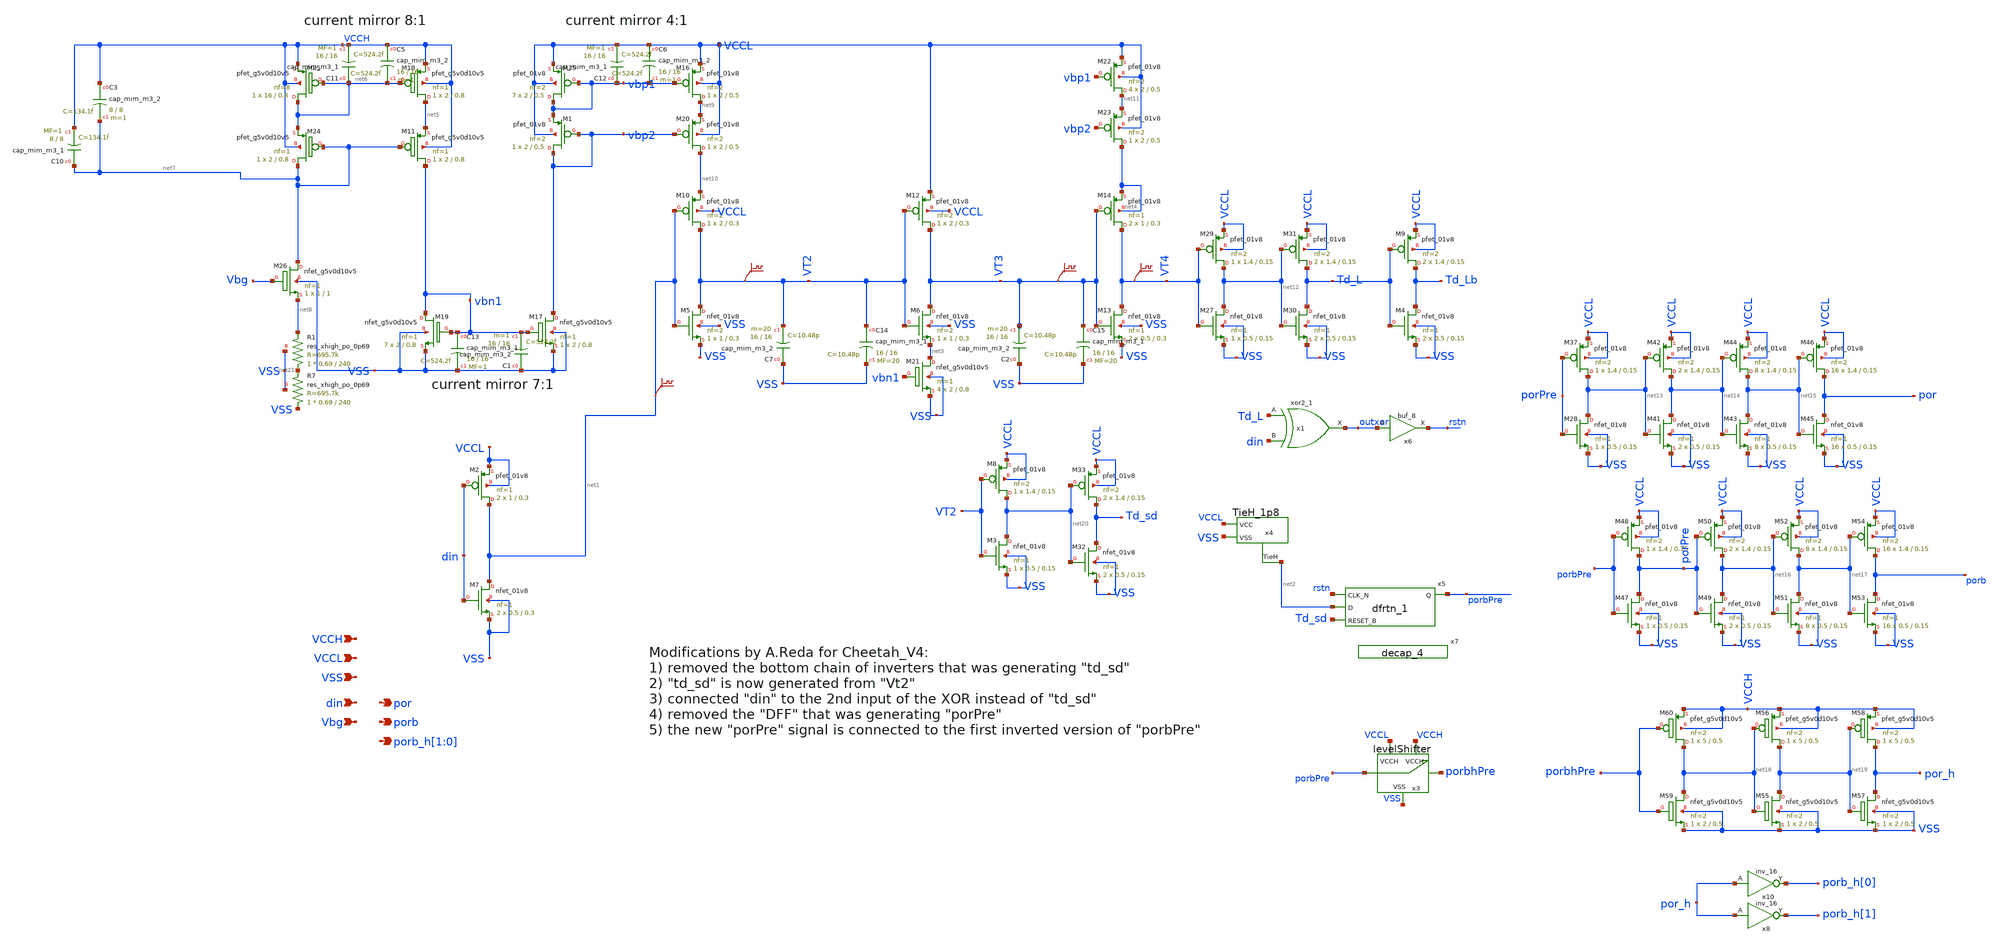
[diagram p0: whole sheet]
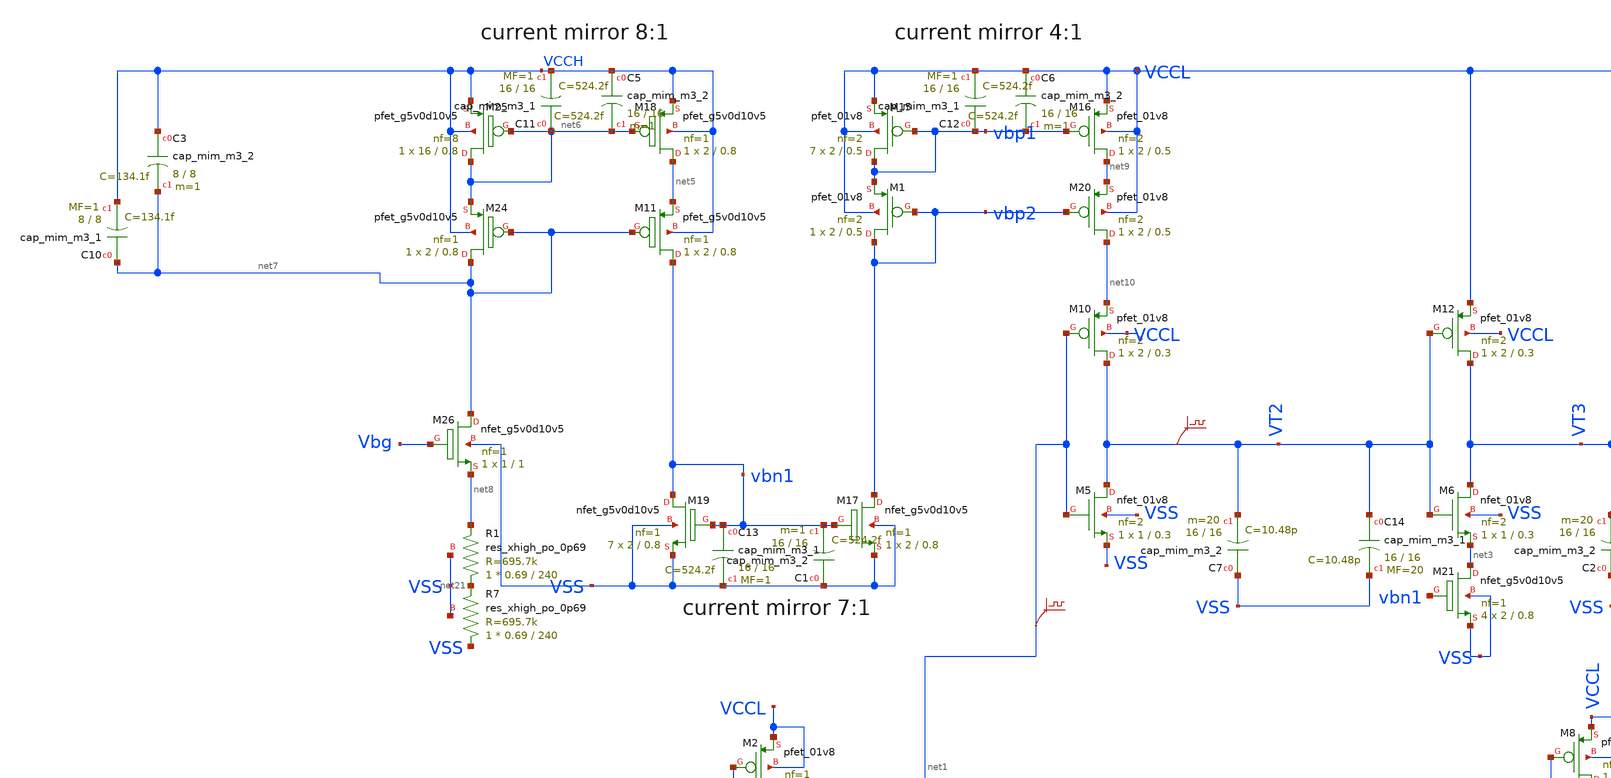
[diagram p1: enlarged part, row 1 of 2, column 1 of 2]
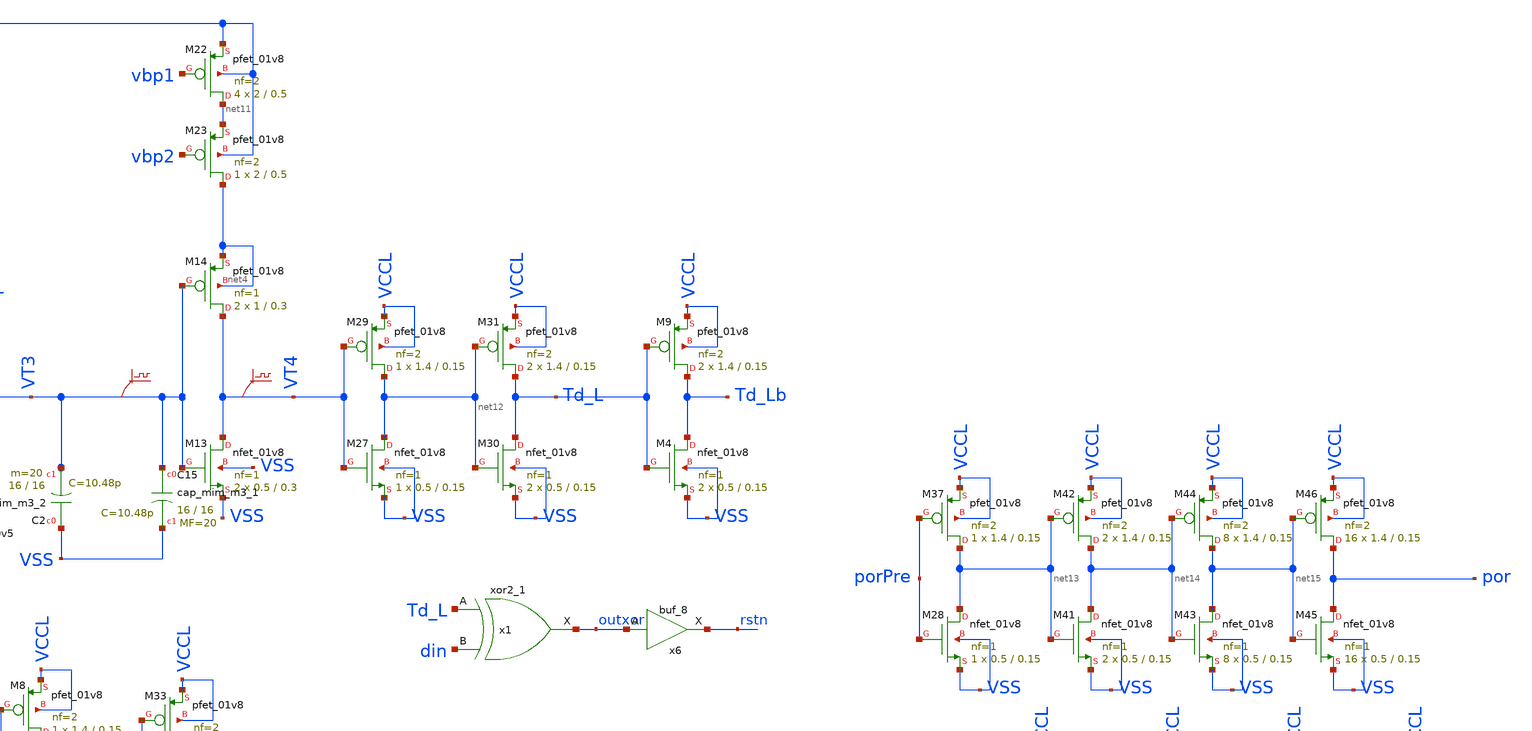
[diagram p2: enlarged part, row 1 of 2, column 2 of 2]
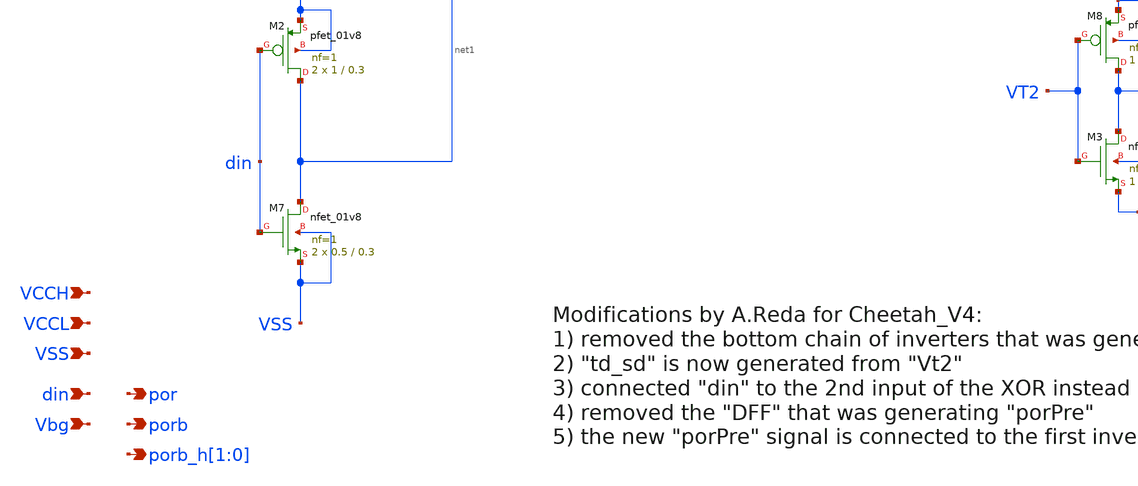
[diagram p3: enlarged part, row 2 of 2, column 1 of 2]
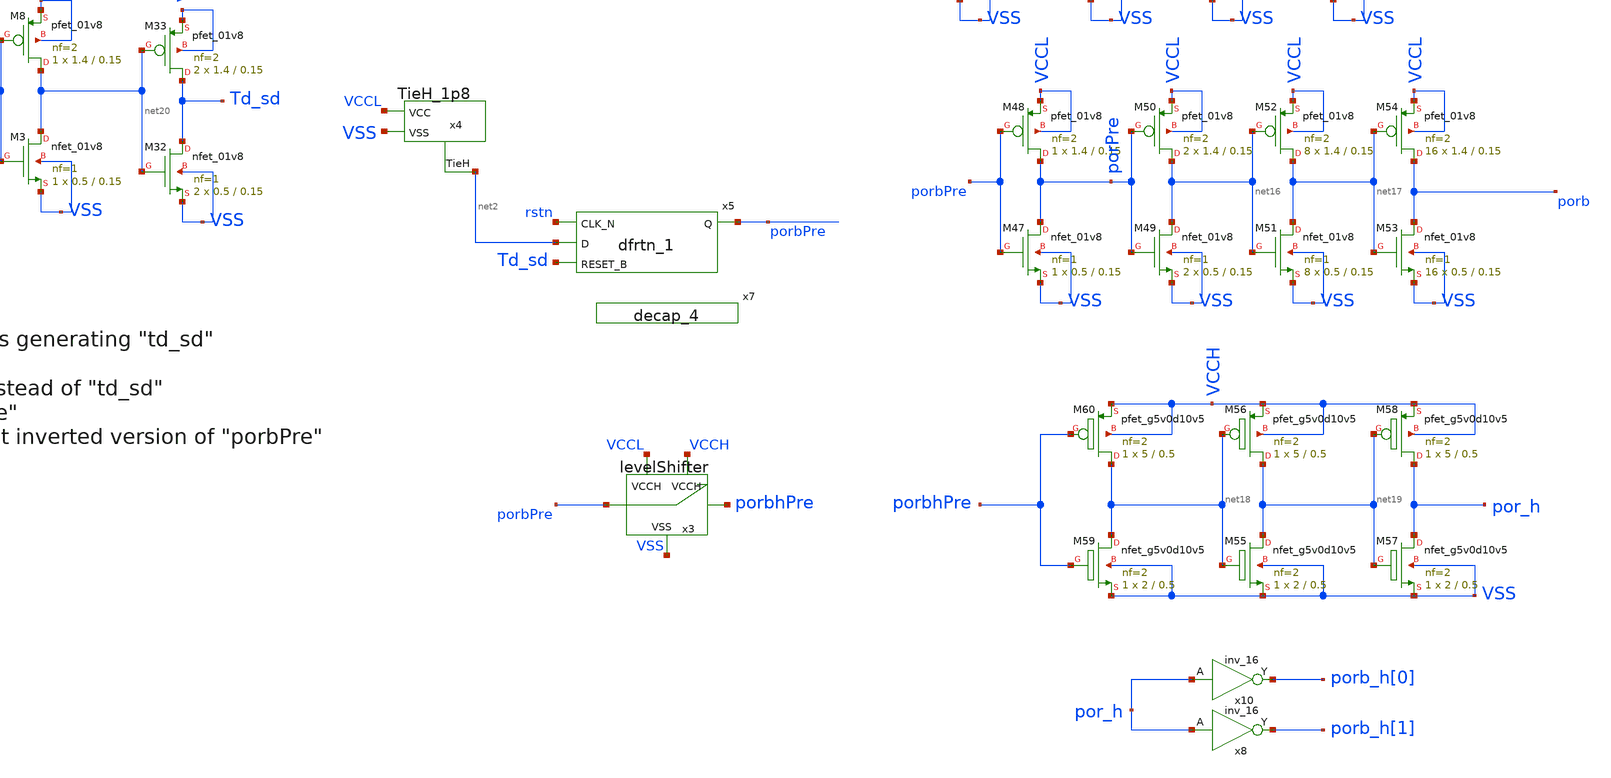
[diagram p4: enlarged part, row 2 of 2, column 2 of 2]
** sch_path: xschem/delayPulse_final.sch
**.subckt delayPulse_final VCCL VSS din Vbg por VCCH porb porb_h[1],porb_h[0]
*.ipin VCCL
*.ipin VSS
*.ipin din
*.ipin Vbg
*.opin por
*.ipin VCCH
*.opin porb
*.opin porb_h[1],porb_h[0]
x1 Td_L din VSS VSS VCCL VCCL outxor sky130_fd_sc_ls__xor2_1
x3 porbPre porbhPre VCCL VSS VCCH levelShifter
XM2 net1 din VCCL VCCL sky130_fd_pr__pfet_01v8 L=0.3 W=1 nf=1 ad='int((nf+1)/2) * W/nf * 0.29' as='int((nf+2)/2) * W/nf * 0.29'
+ pd='2*int((nf+1)/2) * (W/nf + 0.29)' ps='2*int((nf+2)/2) * (W/nf + 0.29)' nrd='0.29 / W' nrs='0.29 / W'
+ sa=0 sb=0 sd=0 mult=2 m=2
XM5 VT2 net1 VSS VSS sky130_fd_pr__nfet_01v8 L=0.3 W=1 nf=2 ad='int((nf+1)/2) * W/nf * 0.29' as='int((nf+2)/2) * W/nf * 0.29'
+ pd='2*int((nf+1)/2) * (W/nf + 0.29)' ps='2*int((nf+2)/2) * (W/nf + 0.29)' nrd='0.29 / W' nrs='0.29 / W'
+ sa=0 sb=0 sd=0 mult=1 m=1
XM7 net1 din VSS VSS sky130_fd_pr__nfet_01v8 L=0.3 W=0.5 nf=1 ad='int((nf+1)/2) * W/nf * 0.29' as='int((nf+2)/2) * W/nf * 0.29'
+ pd='2*int((nf+1)/2) * (W/nf + 0.29)' ps='2*int((nf+2)/2) * (W/nf + 0.29)' nrd='0.29 / W' nrs='0.29 / W'
+ sa=0 sb=0 sd=0 mult=2 m=2
XM10 VT2 net1 net10 VCCL sky130_fd_pr__pfet_01v8 L=0.3 W=2 nf=2 ad='int((nf+1)/2) * W/nf * 0.29' as='int((nf+2)/2) * W/nf * 0.29'
+ pd='2*int((nf+1)/2) * (W/nf + 0.29)' ps='2*int((nf+2)/2) * (W/nf + 0.29)' nrd='0.29 / W' nrs='0.29 / W'
+ sa=0 sb=0 sd=0 mult=1 m=1
XM13 VT4 VT3 VSS VSS sky130_fd_pr__nfet_01v8 L=0.3 W=0.5 nf=1 ad='int((nf+1)/2) * W/nf * 0.29' as='int((nf+2)/2) * W/nf * 0.29'
+ pd='2*int((nf+1)/2) * (W/nf + 0.29)' ps='2*int((nf+2)/2) * (W/nf + 0.29)' nrd='0.29 / W' nrs='0.29 / W'
+ sa=0 sb=0 sd=0 mult=2 m=2
XM14 VT4 VT3 net4 net4 sky130_fd_pr__pfet_01v8 L=0.3 W=1 nf=1 ad='int((nf+1)/2) * W/nf * 0.29' as='int((nf+2)/2) * W/nf * 0.29'
+ pd='2*int((nf+1)/2) * (W/nf + 0.29)' ps='2*int((nf+2)/2) * (W/nf + 0.29)' nrd='0.29 / W' nrs='0.29 / W'
+ sa=0 sb=0 sd=0 mult=2 m=2
x4 net2 VSS VCCL TieH_1p8
XM11 vbn1 net7 net5 VCCH sky130_fd_pr__pfet_g5v0d10v5 L=0.8 W=2 nf=1 ad='int((nf+1)/2) * W/nf * 0.29'
+ as='int((nf+2)/2) * W/nf * 0.29' pd='2*int((nf+1)/2) * (W/nf + 0.29)' ps='2*int((nf+2)/2) * (W/nf + 0.29)'
+ nrd='0.29 / W' nrs='0.29 / W' sa=0 sb=0 sd=0 mult=1 m=1
XM17 vbp2 vbn1 VSS VSS sky130_fd_pr__nfet_g5v0d10v5 L=0.8 W=2 nf=1 ad='int((nf+1)/2) * W/nf * 0.29' as='int((nf+2)/2) * W/nf * 0.29'
+ pd='2*int((nf+1)/2) * (W/nf + 0.29)' ps='2*int((nf+2)/2) * (W/nf + 0.29)' nrd='0.29 / W' nrs='0.29 / W'
+ sa=0 sb=0 sd=0 mult=1 m=1
XM18 net5 net6 VCCH VCCH sky130_fd_pr__pfet_g5v0d10v5 L=0.8 W=2 nf=1 ad='int((nf+1)/2) * W/nf * 0.29'
+ as='int((nf+2)/2) * W/nf * 0.29' pd='2*int((nf+1)/2) * (W/nf + 0.29)' ps='2*int((nf+2)/2) * (W/nf + 0.29)'
+ nrd='0.29 / W' nrs='0.29 / W' sa=0 sb=0 sd=0 mult=1 m=1
XM19 vbn1 vbn1 VSS VSS sky130_fd_pr__nfet_g5v0d10v5 L=0.8 W=2 nf=1 ad='int((nf+1)/2) * W/nf * 0.29' as='int((nf+2)/2) * W/nf * 0.29'
+ pd='2*int((nf+1)/2) * (W/nf + 0.29)' ps='2*int((nf+2)/2) * (W/nf + 0.29)' nrd='0.29 / W' nrs='0.29 / W'
+ sa=0 sb=0 sd=0 mult=7 m=7
XM24 net7 net7 net6 VCCH sky130_fd_pr__pfet_g5v0d10v5 L=0.8 W=2 nf=1 ad='int((nf+1)/2) * W/nf * 0.29'
+ as='int((nf+2)/2) * W/nf * 0.29' pd='2*int((nf+1)/2) * (W/nf + 0.29)' ps='2*int((nf+2)/2) * (W/nf + 0.29)'
+ nrd='0.29 / W' nrs='0.29 / W' sa=0 sb=0 sd=0 mult=1 m=1
XM25 net6 net6 VCCH VCCH sky130_fd_pr__pfet_g5v0d10v5 L=0.8 W=16 nf=8 ad='int((nf+1)/2) * W/nf * 0.29'
+ as='int((nf+2)/2) * W/nf * 0.29' pd='2*int((nf+1)/2) * (W/nf + 0.29)' ps='2*int((nf+2)/2) * (W/nf + 0.29)'
+ nrd='0.29 / W' nrs='0.29 / W' sa=0 sb=0 sd=0 mult=1 m=1
XM26 net7 Vbg net8 VSS sky130_fd_pr__nfet_g5v0d10v5 L=1 W=1 nf=1 ad='int((nf+1)/2) * W/nf * 0.29' as='int((nf+2)/2) * W/nf * 0.29'
+ pd='2*int((nf+1)/2) * (W/nf + 0.29)' ps='2*int((nf+2)/2) * (W/nf + 0.29)' nrd='0.29 / W' nrs='0.29 / W'
+ sa=0 sb=0 sd=0 mult=1 m=1
XM6 VT3 VT2 net3 VSS sky130_fd_pr__nfet_01v8 L=0.3 W=1 nf=2 ad='int((nf+1)/2) * W/nf * 0.29' as='int((nf+2)/2) * W/nf * 0.29'
+ pd='2*int((nf+1)/2) * (W/nf + 0.29)' ps='2*int((nf+2)/2) * (W/nf + 0.29)' nrd='0.29 / W' nrs='0.29 / W'
+ sa=0 sb=0 sd=0 mult=1 m=1
XM12 VT3 VT2 VCCL VCCL sky130_fd_pr__pfet_01v8 L=0.3 W=2 nf=2 ad='int((nf+1)/2) * W/nf * 0.29' as='int((nf+2)/2) * W/nf * 0.29'
+ pd='2*int((nf+1)/2) * (W/nf + 0.29)' ps='2*int((nf+2)/2) * (W/nf + 0.29)' nrd='0.29 / W' nrs='0.29 / W'
+ sa=0 sb=0 sd=0 mult=1 m=1
XM1 vbp2 vbp2 vbp1 VCCL sky130_fd_pr__pfet_01v8 L=0.5 W=2 nf=2 ad='int((nf+1)/2) * W/nf * 0.29' as='int((nf+2)/2) * W/nf * 0.29'
+ pd='2*int((nf+1)/2) * (W/nf + 0.29)' ps='2*int((nf+2)/2) * (W/nf + 0.29)' nrd='0.29 / W' nrs='0.29 / W'
+ sa=0 sb=0 sd=0 mult=1 m=1
XM15 vbp1 vbp1 VCCL VCCL sky130_fd_pr__pfet_01v8 L=0.5 W=2 nf=2 ad='int((nf+1)/2) * W/nf * 0.29' as='int((nf+2)/2) * W/nf * 0.29'
+ pd='2*int((nf+1)/2) * (W/nf + 0.29)' ps='2*int((nf+2)/2) * (W/nf + 0.29)' nrd='0.29 / W' nrs='0.29 / W'
+ sa=0 sb=0 sd=0 mult=7 m=7
XM16 net9 vbp1 VCCL VCCL sky130_fd_pr__pfet_01v8 L=0.5 W=2 nf=2 ad='int((nf+1)/2) * W/nf * 0.29' as='int((nf+2)/2) * W/nf * 0.29'
+ pd='2*int((nf+1)/2) * (W/nf + 0.29)' ps='2*int((nf+2)/2) * (W/nf + 0.29)' nrd='0.29 / W' nrs='0.29 / W'
+ sa=0 sb=0 sd=0 mult=1 m=1
XM20 net10 vbp2 net9 VCCL sky130_fd_pr__pfet_01v8 L=0.5 W=2 nf=2 ad='int((nf+1)/2) * W/nf * 0.29' as='int((nf+2)/2) * W/nf * 0.29'
+ pd='2*int((nf+1)/2) * (W/nf + 0.29)' ps='2*int((nf+2)/2) * (W/nf + 0.29)' nrd='0.29 / W' nrs='0.29 / W'
+ sa=0 sb=0 sd=0 mult=1 m=1
XM21 net3 vbn1 VSS VSS sky130_fd_pr__nfet_g5v0d10v5 L=0.8 W=2 nf=1 ad='int((nf+1)/2) * W/nf * 0.29' as='int((nf+2)/2) * W/nf * 0.29'
+ pd='2*int((nf+1)/2) * (W/nf + 0.29)' ps='2*int((nf+2)/2) * (W/nf + 0.29)' nrd='0.29 / W' nrs='0.29 / W'
+ sa=0 sb=0 sd=0 mult=4 m=4
XM22 net11 vbp1 VCCL VCCL sky130_fd_pr__pfet_01v8 L=0.5 W=2 nf=2 ad='int((nf+1)/2) * W/nf * 0.29' as='int((nf+2)/2) * W/nf * 0.29'
+ pd='2*int((nf+1)/2) * (W/nf + 0.29)' ps='2*int((nf+2)/2) * (W/nf + 0.29)' nrd='0.29 / W' nrs='0.29 / W'
+ sa=0 sb=0 sd=0 mult=4 m=4
XM23 net4 vbp2 net11 VCCL sky130_fd_pr__pfet_01v8 L=0.5 W=2 nf=2 ad='int((nf+1)/2) * W/nf * 0.29' as='int((nf+2)/2) * W/nf * 0.29'
+ pd='2*int((nf+1)/2) * (W/nf + 0.29)' ps='2*int((nf+2)/2) * (W/nf + 0.29)' nrd='0.29 / W' nrs='0.29 / W'
+ sa=0 sb=0 sd=0 mult=1 m=1
XM27 net12 VT4 VSS VSS sky130_fd_pr__nfet_01v8 L=0.15 W=0.5 nf=1 ad='int((nf+1)/2) * W/nf * 0.29' as='int((nf+2)/2) * W/nf * 0.29'
+ pd='2*int((nf+1)/2) * (W/nf + 0.29)' ps='2*int((nf+2)/2) * (W/nf + 0.29)' nrd='0.29 / W' nrs='0.29 / W'
+ sa=0 sb=0 sd=0 mult=1 m=1
XM29 net12 VT4 VCCL VCCL sky130_fd_pr__pfet_01v8 L=0.15 W=1.4 nf=2 ad='int((nf+1)/2) * W/nf * 0.29' as='int((nf+2)/2) * W/nf * 0.29'
+ pd='2*int((nf+1)/2) * (W/nf + 0.29)' ps='2*int((nf+2)/2) * (W/nf + 0.29)' nrd='0.29 / W' nrs='0.29 / W'
+ sa=0 sb=0 sd=0 mult=1 m=1
XM30 Td_L net12 VSS VSS sky130_fd_pr__nfet_01v8 L=0.15 W=0.5 nf=1 ad='int((nf+1)/2) * W/nf * 0.29' as='int((nf+2)/2) * W/nf * 0.29'
+ pd='2*int((nf+1)/2) * (W/nf + 0.29)' ps='2*int((nf+2)/2) * (W/nf + 0.29)' nrd='0.29 / W' nrs='0.29 / W'
+ sa=0 sb=0 sd=0 mult=2 m=2
XM31 Td_L net12 VCCL VCCL sky130_fd_pr__pfet_01v8 L=0.15 W=1.4 nf=2 ad='int((nf+1)/2) * W/nf * 0.29'
+ as='int((nf+2)/2) * W/nf * 0.29' pd='2*int((nf+1)/2) * (W/nf + 0.29)' ps='2*int((nf+2)/2) * (W/nf + 0.29)'
+ nrd='0.29 / W' nrs='0.29 / W' sa=0 sb=0 sd=0 mult=2 m=2
x6 outxor VSS VSS VCCL VCCL rstn sky130_fd_sc_ls__buf_8
XC7 VSS VT2 sky130_fd_pr__cap_mim_m3_2 W=16 L=16 MF=20 m=20
XC2 VSS VT3 sky130_fd_pr__cap_mim_m3_2 W=16 L=16 MF=20 m=20
x5 rstn net2 Td_sd VSS VSS VCCL VCCL porbPre sky130_fd_sc_ls__dfrtn_1
XM4 Td_Lb Td_L VSS VSS sky130_fd_pr__nfet_01v8 L=0.15 W=0.5 nf=1 ad='int((nf+1)/2) * W/nf * 0.29' as='int((nf+2)/2) * W/nf * 0.29'
+ pd='2*int((nf+1)/2) * (W/nf + 0.29)' ps='2*int((nf+2)/2) * (W/nf + 0.29)' nrd='0.29 / W' nrs='0.29 / W'
+ sa=0 sb=0 sd=0 mult=2 m=2
XM9 Td_Lb Td_L VCCL VCCL sky130_fd_pr__pfet_01v8 L=0.15 W=1.4 nf=2 ad='int((nf+1)/2) * W/nf * 0.29' as='int((nf+2)/2) * W/nf * 0.29'
+ pd='2*int((nf+1)/2) * (W/nf + 0.29)' ps='2*int((nf+2)/2) * (W/nf + 0.29)' nrd='0.29 / W' nrs='0.29 / W'
+ sa=0 sb=0 sd=0 mult=2 m=2
XC1 VSS vbn1 sky130_fd_pr__cap_mim_m3_2 W=16 L=16 MF=1 m=1
XC5 VCCH net6 sky130_fd_pr__cap_mim_m3_2 W=16 L=16 MF=1 m=1
XC6 VCCL vbp1 sky130_fd_pr__cap_mim_m3_2 W=16 L=16 MF=1 m=1
XC3 VCCH net7 sky130_fd_pr__cap_mim_m3_2 W=8 L=8 MF=1 m=1
XM28 net13 porPre VSS VSS sky130_fd_pr__nfet_01v8 L=0.15 W=0.5 nf=1 ad='int((nf+1)/2) * W/nf * 0.29'
+ as='int((nf+2)/2) * W/nf * 0.29' pd='2*int((nf+1)/2) * (W/nf + 0.29)' ps='2*int((nf+2)/2) * (W/nf + 0.29)'
+ nrd='0.29 / W' nrs='0.29 / W' sa=0 sb=0 sd=0 mult=1 m=1
XM37 net13 porPre VCCL VCCL sky130_fd_pr__pfet_01v8 L=0.15 W=1.4 nf=2 ad='int((nf+1)/2) * W/nf * 0.29'
+ as='int((nf+2)/2) * W/nf * 0.29' pd='2*int((nf+1)/2) * (W/nf + 0.29)' ps='2*int((nf+2)/2) * (W/nf + 0.29)'
+ nrd='0.29 / W' nrs='0.29 / W' sa=0 sb=0 sd=0 mult=1 m=1
XM41 net14 net13 VSS VSS sky130_fd_pr__nfet_01v8 L=0.15 W=0.5 nf=1 ad='int((nf+1)/2) * W/nf * 0.29' as='int((nf+2)/2) * W/nf * 0.29'
+ pd='2*int((nf+1)/2) * (W/nf + 0.29)' ps='2*int((nf+2)/2) * (W/nf + 0.29)' nrd='0.29 / W' nrs='0.29 / W'
+ sa=0 sb=0 sd=0 mult=2 m=2
XM42 net14 net13 VCCL VCCL sky130_fd_pr__pfet_01v8 L=0.15 W=1.4 nf=2 ad='int((nf+1)/2) * W/nf * 0.29'
+ as='int((nf+2)/2) * W/nf * 0.29' pd='2*int((nf+1)/2) * (W/nf + 0.29)' ps='2*int((nf+2)/2) * (W/nf + 0.29)'
+ nrd='0.29 / W' nrs='0.29 / W' sa=0 sb=0 sd=0 mult=2 m=2
XM43 net15 net14 VSS VSS sky130_fd_pr__nfet_01v8 L=0.15 W=0.5 nf=1 ad='int((nf+1)/2) * W/nf * 0.29' as='int((nf+2)/2) * W/nf * 0.29'
+ pd='2*int((nf+1)/2) * (W/nf + 0.29)' ps='2*int((nf+2)/2) * (W/nf + 0.29)' nrd='0.29 / W' nrs='0.29 / W'
+ sa=0 sb=0 sd=0 mult=8 m=8
XM44 net15 net14 VCCL VCCL sky130_fd_pr__pfet_01v8 L=0.15 W=1.4 nf=2 ad='int((nf+1)/2) * W/nf * 0.29'
+ as='int((nf+2)/2) * W/nf * 0.29' pd='2*int((nf+1)/2) * (W/nf + 0.29)' ps='2*int((nf+2)/2) * (W/nf + 0.29)'
+ nrd='0.29 / W' nrs='0.29 / W' sa=0 sb=0 sd=0 mult=8 m=8
XM45 por net15 VSS VSS sky130_fd_pr__nfet_01v8 L=0.15 W=0.5 nf=1 ad='int((nf+1)/2) * W/nf * 0.29' as='int((nf+2)/2) * W/nf * 0.29'
+ pd='2*int((nf+1)/2) * (W/nf + 0.29)' ps='2*int((nf+2)/2) * (W/nf + 0.29)' nrd='0.29 / W' nrs='0.29 / W'
+ sa=0 sb=0 sd=0 mult=16 m=16
XM46 por net15 VCCL VCCL sky130_fd_pr__pfet_01v8 L=0.15 W=1.4 nf=2 ad='int((nf+1)/2) * W/nf * 0.29' as='int((nf+2)/2) * W/nf * 0.29'
+ pd='2*int((nf+1)/2) * (W/nf + 0.29)' ps='2*int((nf+2)/2) * (W/nf + 0.29)' nrd='0.29 / W' nrs='0.29 / W'
+ sa=0 sb=0 sd=0 mult=16 m=16
XM47 porPre porbPre VSS VSS sky130_fd_pr__nfet_01v8 L=0.15 W=0.5 nf=1 ad='int((nf+1)/2) * W/nf * 0.29'
+ as='int((nf+2)/2) * W/nf * 0.29' pd='2*int((nf+1)/2) * (W/nf + 0.29)' ps='2*int((nf+2)/2) * (W/nf + 0.29)'
+ nrd='0.29 / W' nrs='0.29 / W' sa=0 sb=0 sd=0 mult=1 m=1
XM48 porPre porbPre VCCL VCCL sky130_fd_pr__pfet_01v8 L=0.15 W=1.4 nf=2 ad='int((nf+1)/2) * W/nf * 0.29'
+ as='int((nf+2)/2) * W/nf * 0.29' pd='2*int((nf+1)/2) * (W/nf + 0.29)' ps='2*int((nf+2)/2) * (W/nf + 0.29)'
+ nrd='0.29 / W' nrs='0.29 / W' sa=0 sb=0 sd=0 mult=1 m=1
XM49 net16 porPre VSS VSS sky130_fd_pr__nfet_01v8 L=0.15 W=0.5 nf=1 ad='int((nf+1)/2) * W/nf * 0.29'
+ as='int((nf+2)/2) * W/nf * 0.29' pd='2*int((nf+1)/2) * (W/nf + 0.29)' ps='2*int((nf+2)/2) * (W/nf + 0.29)'
+ nrd='0.29 / W' nrs='0.29 / W' sa=0 sb=0 sd=0 mult=2 m=2
XM50 net16 porPre VCCL VCCL sky130_fd_pr__pfet_01v8 L=0.15 W=1.4 nf=2 ad='int((nf+1)/2) * W/nf * 0.29'
+ as='int((nf+2)/2) * W/nf * 0.29' pd='2*int((nf+1)/2) * (W/nf + 0.29)' ps='2*int((nf+2)/2) * (W/nf + 0.29)'
+ nrd='0.29 / W' nrs='0.29 / W' sa=0 sb=0 sd=0 mult=2 m=2
XM51 net17 net16 VSS VSS sky130_fd_pr__nfet_01v8 L=0.15 W=0.5 nf=1 ad='int((nf+1)/2) * W/nf * 0.29' as='int((nf+2)/2) * W/nf * 0.29'
+ pd='2*int((nf+1)/2) * (W/nf + 0.29)' ps='2*int((nf+2)/2) * (W/nf + 0.29)' nrd='0.29 / W' nrs='0.29 / W'
+ sa=0 sb=0 sd=0 mult=8 m=8
XM52 net17 net16 VCCL VCCL sky130_fd_pr__pfet_01v8 L=0.15 W=1.4 nf=2 ad='int((nf+1)/2) * W/nf * 0.29'
+ as='int((nf+2)/2) * W/nf * 0.29' pd='2*int((nf+1)/2) * (W/nf + 0.29)' ps='2*int((nf+2)/2) * (W/nf + 0.29)'
+ nrd='0.29 / W' nrs='0.29 / W' sa=0 sb=0 sd=0 mult=8 m=8
XM53 porb net17 VSS VSS sky130_fd_pr__nfet_01v8 L=0.15 W=0.5 nf=1 ad='int((nf+1)/2) * W/nf * 0.29' as='int((nf+2)/2) * W/nf * 0.29'
+ pd='2*int((nf+1)/2) * (W/nf + 0.29)' ps='2*int((nf+2)/2) * (W/nf + 0.29)' nrd='0.29 / W' nrs='0.29 / W'
+ sa=0 sb=0 sd=0 mult=16 m=16
XM54 porb net17 VCCL VCCL sky130_fd_pr__pfet_01v8 L=0.15 W=1.4 nf=2 ad='int((nf+1)/2) * W/nf * 0.29'
+ as='int((nf+2)/2) * W/nf * 0.29' pd='2*int((nf+1)/2) * (W/nf + 0.29)' ps='2*int((nf+2)/2) * (W/nf + 0.29)'
+ nrd='0.29 / W' nrs='0.29 / W' sa=0 sb=0 sd=0 mult=16 m=16
XM59 net18 porbhPre VSS VSS sky130_fd_pr__nfet_g5v0d10v5 L=0.5 W=2 nf=2 ad='int((nf+1)/2) * W/nf * 0.29'
+ as='int((nf+2)/2) * W/nf * 0.29' pd='2*int((nf+1)/2) * (W/nf + 0.29)' ps='2*int((nf+2)/2) * (W/nf + 0.29)'
+ nrd='0.29 / W' nrs='0.29 / W' sa=0 sb=0 sd=0 mult=1 m=1
XM60 net18 porbhPre VCCH VCCH sky130_fd_pr__pfet_g5v0d10v5 L=0.5 W=5 nf=2 ad='int((nf+1)/2) * W/nf * 0.29'
+ as='int((nf+2)/2) * W/nf * 0.29' pd='2*int((nf+1)/2) * (W/nf + 0.29)' ps='2*int((nf+2)/2) * (W/nf + 0.29)'
+ nrd='0.29 / W' nrs='0.29 / W' sa=0 sb=0 sd=0 mult=1 m=1
x7 VSS VSS VCCL VCCL sky130_fd_sc_ls__decap_4
XC10 net7 VCCH sky130_fd_pr__cap_mim_m3_1 W=8 L=8 MF=1 m=1
XC11 net6 VCCH sky130_fd_pr__cap_mim_m3_1 W=16 L=16 MF=1 m=1
XC12 vbp1 VCCL sky130_fd_pr__cap_mim_m3_1 W=16 L=16 MF=1 m=1
XC13 vbn1 VSS sky130_fd_pr__cap_mim_m3_1 W=16 L=16 MF=1 m=1
XC14 VT2 VSS sky130_fd_pr__cap_mim_m3_1 W=16 L=16 MF=20 m=20
XC15 VT3 VSS sky130_fd_pr__cap_mim_m3_1 W=16 L=16 MF=20 m=20
XR1 net21 net8 VSS sky130_fd_pr__res_xhigh_po_0p69 L=240 mult=1 m=1
XR7 VSS net21 VSS sky130_fd_pr__res_xhigh_po_0p69 L=240 mult=1 m=1
XM55 net19 net18 VSS VSS sky130_fd_pr__nfet_g5v0d10v5 L=0.5 W=2 nf=2 ad='int((nf+1)/2) * W/nf * 0.29'
+ as='int((nf+2)/2) * W/nf * 0.29' pd='2*int((nf+1)/2) * (W/nf + 0.29)' ps='2*int((nf+2)/2) * (W/nf + 0.29)'
+ nrd='0.29 / W' nrs='0.29 / W' sa=0 sb=0 sd=0 mult=1 m=1
XM56 net19 net18 VCCH VCCH sky130_fd_pr__pfet_g5v0d10v5 L=0.5 W=5 nf=2 ad='int((nf+1)/2) * W/nf * 0.29'
+ as='int((nf+2)/2) * W/nf * 0.29' pd='2*int((nf+1)/2) * (W/nf + 0.29)' ps='2*int((nf+2)/2) * (W/nf + 0.29)'
+ nrd='0.29 / W' nrs='0.29 / W' sa=0 sb=0 sd=0 mult=1 m=1
XM57 por_h net19 VSS VSS sky130_fd_pr__nfet_g5v0d10v5 L=0.5 W=2 nf=2 ad='int((nf+1)/2) * W/nf * 0.29'
+ as='int((nf+2)/2) * W/nf * 0.29' pd='2*int((nf+1)/2) * (W/nf + 0.29)' ps='2*int((nf+2)/2) * (W/nf + 0.29)'
+ nrd='0.29 / W' nrs='0.29 / W' sa=0 sb=0 sd=0 mult=1 m=1
XM58 por_h net19 VCCH VCCH sky130_fd_pr__pfet_g5v0d10v5 L=0.5 W=5 nf=2 ad='int((nf+1)/2) * W/nf * 0.29'
+ as='int((nf+2)/2) * W/nf * 0.29' pd='2*int((nf+1)/2) * (W/nf + 0.29)' ps='2*int((nf+2)/2) * (W/nf + 0.29)'
+ nrd='0.29 / W' nrs='0.29 / W' sa=0 sb=0 sd=0 mult=1 m=1
x10 por_h VSS VSS VCCH VCCH porb_h[0] sky130_fd_sc_hvl__inv_16
x8 por_h VSS VSS VCCH VCCH porb_h[1] sky130_fd_sc_hvl__inv_16
.save v(vt2)
.save v(net1)
.save v(vt3)
.save v(vt4)
XM3 net20 VT2 VSS VSS sky130_fd_pr__nfet_01v8 L=0.15 W=0.5 nf=1 ad='int((nf+1)/2) * W/nf * 0.29' as='int((nf+2)/2) * W/nf * 0.29'
+ pd='2*int((nf+1)/2) * (W/nf + 0.29)' ps='2*int((nf+2)/2) * (W/nf + 0.29)' nrd='0.29 / W' nrs='0.29 / W'
+ sa=0 sb=0 sd=0 mult=1 m=1
XM8 net20 VT2 VCCL VCCL sky130_fd_pr__pfet_01v8 L=0.15 W=1.4 nf=2 ad='int((nf+1)/2) * W/nf * 0.29' as='int((nf+2)/2) * W/nf * 0.29'
+ pd='2*int((nf+1)/2) * (W/nf + 0.29)' ps='2*int((nf+2)/2) * (W/nf + 0.29)' nrd='0.29 / W' nrs='0.29 / W'
+ sa=0 sb=0 sd=0 mult=1 m=1
XM32 Td_sd net20 VSS VSS sky130_fd_pr__nfet_01v8 L=0.15 W=0.5 nf=1 ad='int((nf+1)/2) * W/nf * 0.29' as='int((nf+2)/2) * W/nf * 0.29'
+ pd='2*int((nf+1)/2) * (W/nf + 0.29)' ps='2*int((nf+2)/2) * (W/nf + 0.29)' nrd='0.29 / W' nrs='0.29 / W'
+ sa=0 sb=0 sd=0 mult=2 m=2
XM33 Td_sd net20 VCCL VCCL sky130_fd_pr__pfet_01v8 L=0.15 W=1.4 nf=2 ad='int((nf+1)/2) * W/nf * 0.29'
+ as='int((nf+2)/2) * W/nf * 0.29' pd='2*int((nf+1)/2) * (W/nf + 0.29)' ps='2*int((nf+2)/2) * (W/nf + 0.29)'
+ nrd='0.29 / W' nrs='0.29 / W' sa=0 sb=0 sd=0 mult=2 m=2
**.ends
.end
